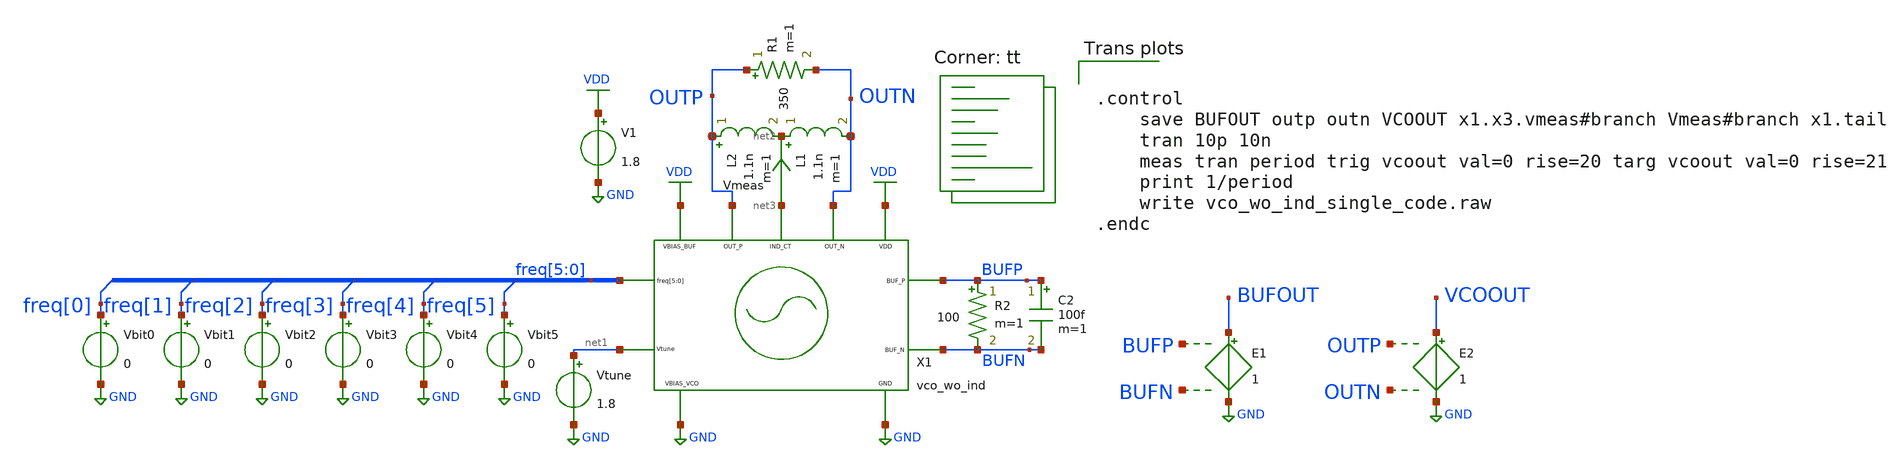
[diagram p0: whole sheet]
** sch_path: xschem/vco/testbenches/top/vco_wo_ind_single_code.sch
* YI/C9Shc8z/CWPKLJb8BQD+O4ziO4wpAwbu7u7s7HEAy2IIt2IIlQD6O4ziO4ypAAICtDl/GPL8AgNZy7Go7vwAAAAAAAAAAAAAAAAAAAAAAAPeMn2NHvywNosQhFFq
**.subckt vco_wo_ind_single_code
V1 VDD GND 1.8
Vbit0 freq[0] GND 0
Vbit1 freq[1] GND 0
Vbit2 freq[2] GND 0
Vbit3 freq[3] GND 0
Vbit4 freq[4] GND 0
Vbit5 freq[5] GND 0
L1 net2 OUTN 1.1n m=1
L2 OUTP net2 1.1n m=1
Vtune net1 GND 1.8
R1 OUTP OUTN 350 m=1
R2 BUFP BUFN 100 m=1
C2 BUFP BUFN 100f m=1
E1 BUFOUT GND BUFP BUFN 1
E2 VCOOUT GND OUTP OUTN 1
X1 OUTP GND net3 VDD OUTN freq[5] freq[4] freq[3] freq[2] freq[1] freq[0] GND net1 BUFP BUFN VDD
+ vco_wo_ind
Vmeas net3 net2 0
.save i(vmeas)
**** begin user architecture code


.control
    save BUFOUT outp outn VCOOUT x1.x3.vmeas#branch Vmeas#branch x1.tail
    tran 10p 10n
    meas tran period trig vcoout val=0 rise=20 targ vcoout val=0 rise=21
    print 1/period
    write vco_wo_ind_single_code.raw
.endc


.lib $::SKYWATER_MODELS/sky130.lib.spice tt
**** end user architecture code
**.ends
.GLOBAL GND
.GLOBAL VDD
.end
